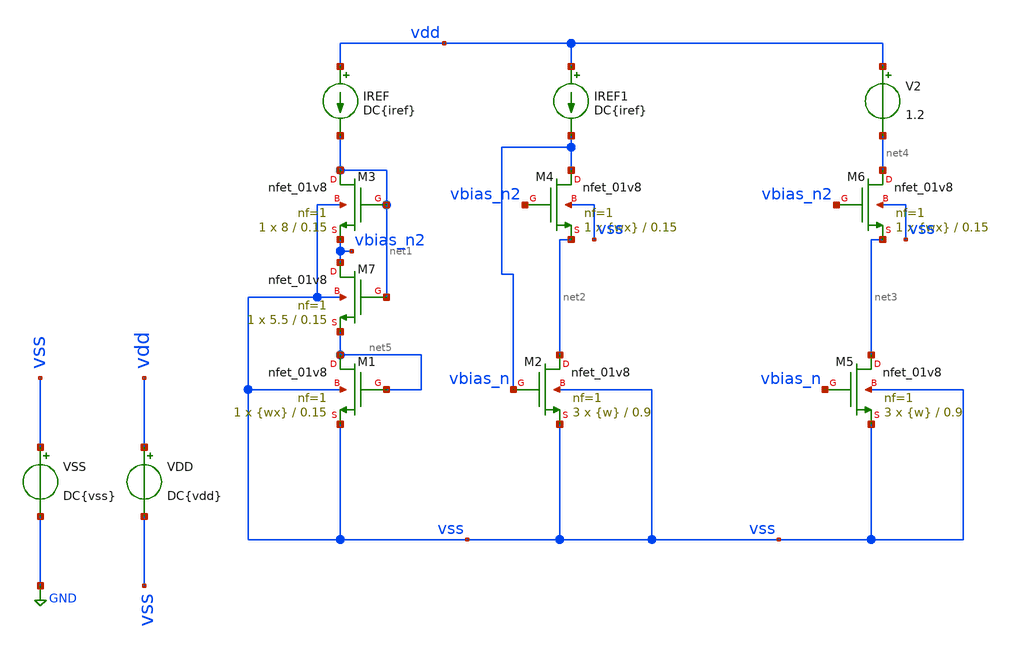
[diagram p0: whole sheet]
** sch_path: tp2/tp2_3b.sch
**.subckt tp2_3b
XM1 net5 net5 vss vss sky130_fd_pr__nfet_01v8 L=0.15 W={wx} nf=1 ad='int((nf+1)/2) * W/nf * 0.29' as='int((nf+2)/2) * W/nf * 0.29'
+ pd='2*int((nf+1)/2) * (W/nf + 0.29)' ps='2*int((nf+2)/2) * (W/nf + 0.29)' nrd='0.29 / W' nrs='0.29 / W'
+ sa=0 sb=0 sd=0 mult=1 m=1
XM2 net2 vbias_n vss vss sky130_fd_pr__nfet_01v8 L=0.9 W={w} nf=1 ad='int((nf+1)/2) * W/nf * 0.29' as='int((nf+2)/2) * W/nf * 0.29'
+ pd='2*int((nf+1)/2) * (W/nf + 0.29)' ps='2*int((nf+2)/2) * (W/nf + 0.29)' nrd='0.29 / W' nrs='0.29 / W'
+ sa=0 sb=0 sd=0 mult=3 m=3
IREF vdd net1 DC{iref}
VSS vss GND DC{vss}
VDD vdd vss DC{vdd}
XM3 net1 net1 vbias_n2 vss sky130_fd_pr__nfet_01v8 L=0.15 W=8 nf=1 ad='int((nf+1)/2) * W/nf * 0.29' as='int((nf+2)/2) * W/nf * 0.29'
+ pd='2*int((nf+1)/2) * (W/nf + 0.29)' ps='2*int((nf+2)/2) * (W/nf + 0.29)' nrd='0.29 / W' nrs='0.29 / W'
+ sa=0 sb=0 sd=0 mult=1 m=1
XM4 vbias_n vbias_n2 net2 vss sky130_fd_pr__nfet_01v8 L=0.15 W={wx} nf=1 ad='int((nf+1)/2) * W/nf * 0.29'
+ as='int((nf+2)/2) * W/nf * 0.29' pd='2*int((nf+1)/2) * (W/nf + 0.29)' ps='2*int((nf+2)/2) * (W/nf + 0.29)'
+ nrd='0.29 / W' nrs='0.29 / W' sa=0 sb=0 sd=0 mult=1 m=1
XM5 net3 vbias_n vss vss sky130_fd_pr__nfet_01v8 L=0.9 W={w} nf=1 ad='int((nf+1)/2) * W/nf * 0.29' as='int((nf+2)/2) * W/nf * 0.29'
+ pd='2*int((nf+1)/2) * (W/nf + 0.29)' ps='2*int((nf+2)/2) * (W/nf + 0.29)' nrd='0.29 / W' nrs='0.29 / W'
+ sa=0 sb=0 sd=0 mult=3 m=3
XM6 net4 vbias_n2 net3 vss sky130_fd_pr__nfet_01v8 L=0.15 W={wx} nf=1 ad='int((nf+1)/2) * W/nf * 0.29'
+ as='int((nf+2)/2) * W/nf * 0.29' pd='2*int((nf+1)/2) * (W/nf + 0.29)' ps='2*int((nf+2)/2) * (W/nf + 0.29)'
+ nrd='0.29 / W' nrs='0.29 / W' sa=0 sb=0 sd=0 mult=1 m=1
V2 vdd net4 1.2
IREF1 vdd vbias_n DC{iref}
XM7 vbias_n2 net1 net5 vss sky130_fd_pr__nfet_01v8 L=0.15 W=5.5 nf=1 ad='int((nf+1)/2) * W/nf * 0.29'
+ as='int((nf+2)/2) * W/nf * 0.29' pd='2*int((nf+1)/2) * (W/nf + 0.29)' ps='2*int((nf+2)/2) * (W/nf + 0.29)'
+ nrd='0.29 / W' nrs='0.29 / W' sa=0 sb=0 sd=0 mult=1 m=1
**** begin user architecture code



* Parameters
.param vdd = 1.8
.param vss = 0.0
.param iref = 200u
.param w = 90
.param wx = 70
.options TEMPS = 27.0

* Models
*.lib ~/skywater/skywater-pdk/libraries/sky130_fd_pr_ngspice/latest/models/corners/sky130.lib TT
.lib /foss/pdks/sky130A/libs.tech/ngspice/sky130.lib.spice ff
* Data to save
.save all  @M.XM1.msky130_fd_pr__nfet_01v8[id]  @M.XM1.msky130_fd_pr__nfet_01v8[gm]  @M.XM1.msky130_fd_pr__nfet_01v8[vds]  @M.XM1.msky130_fd_pr__nfet_01v8[vgs]  @M.XM1.msky130_fd_pr__nfet_01v8[w]  @M.XM1.msky130_fd_pr__nfet_01v8[vth]  @M.XM2.msky130_fd_pr__nfet_01v8[id]  @M.XM2.msky130_fd_pr__nfet_01v8[gm]  @M.XM2.msky130_fd_pr__nfet_01v8[vds]  @M.XM2.msky130_fd_pr__nfet_01v8[vgs]  @M.XM2.msky130_fd_pr__nfet_01v8[w]  @M.XM2.msky130_fd_pr__nfet_01v8[vth]  @M.XM2.msky130_fd_pr__nfet_01v8[vdsat]  @M.XM4.msky130_fd_pr__nfet_01v8[vdsat]  @M.XM7.msky130_fd_pr__nfet_01v8[vdsat]  @M.XM6.msky130_fd_pr__nfet_01v8[vdsat]  @M.XM5.msky130_fd_pr__nfet_01v8[vth]  @M.XM4.msky130_fd_pr__nfet_01v8[vth]  @M.XM1.msky130_fd_pr__nfet_01v8[vth]  @M.XM3.msky130_fd_pr__nfet_01v8[vth]  @M.XM7.msky130_fd_pr__nfet_01v8[vth]  @M.XM6.msky130_fd_pr__nfet_01v8[vth]
* Simulation
.control

  op
  save all
  unset filetype
  write tp2_3b.raw

.endc

.end


**** end user architecture code
**.ends
.GLOBAL GND
.end
